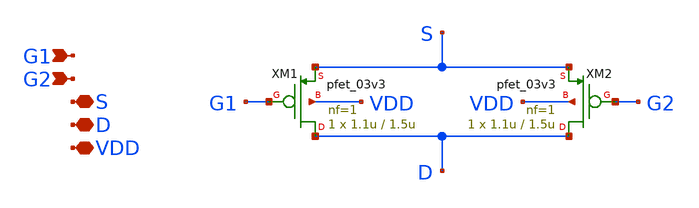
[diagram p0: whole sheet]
** sch_path: designs/libs/core_analog/cp_sym_load/cp_sym_load.sch
**.subckt cp_sym_load G1 G2 S D VDD
*.ipin G1
*.ipin G2
*.iopin S
*.iopin D
*.iopin VDD
XM1 D G1 S VDD pfet_03v3 L=1.5u W=1.1u nf=1 ad='int((nf+1)/2) * W/nf * 0.18u' as='int((nf+2)/2) * W/nf * 0.18u'
+ pd='2*int((nf+1)/2) * (W/nf + 0.18u)' ps='2*int((nf+2)/2) * (W/nf + 0.18u)' nrd='0.18u / W' nrs='0.18u / W'
+ sa=0 sb=0 sd=0 m=1
XM2 D G2 S VDD pfet_03v3 L=1.5u W=1.1u nf=1 ad='int((nf+1)/2) * W/nf * 0.18u' as='int((nf+2)/2) * W/nf * 0.18u'
+ pd='2*int((nf+1)/2) * (W/nf + 0.18u)' ps='2*int((nf+2)/2) * (W/nf + 0.18u)' nrd='0.18u / W' nrs='0.18u / W'
+ sa=0 sb=0 sd=0 m=1
**.ends
.end
